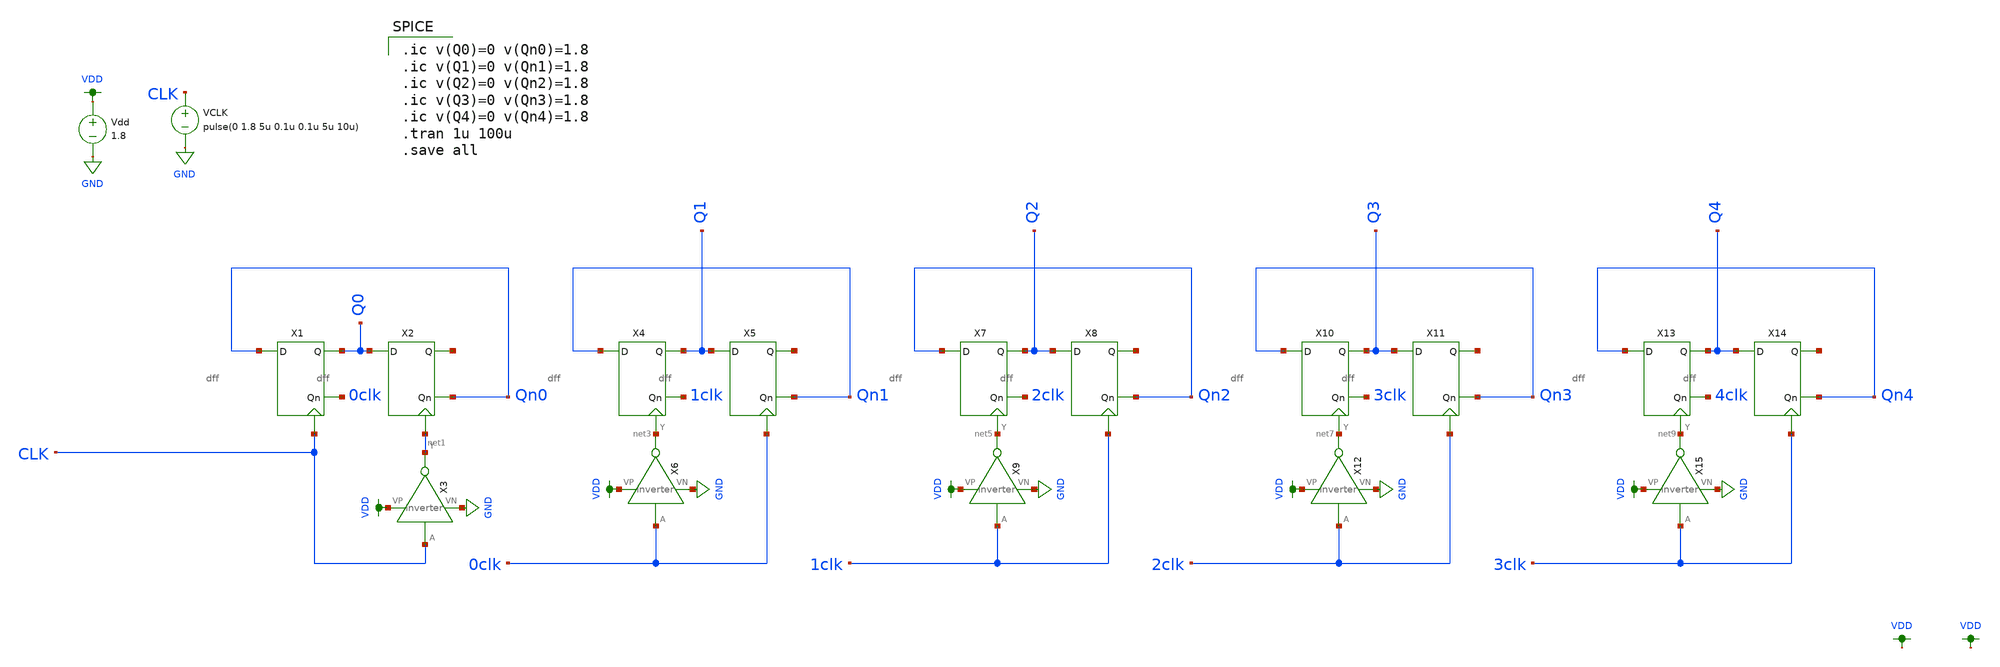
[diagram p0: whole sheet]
** sch_path: schematic/counter_new.sch
**.subckt counter_new
Vdd VDD GND 1.8
VCLK CLK GND pulse(0 1.8 5u 0.1u 0.1u 5u 10u)
X1 Qn0 0clk Q0 CLK dff
X2 Q0 Qn0 net2 net1 dff
X3 CLK net1 VDD GND inverter
X4 Qn1 1clk Q1 net3 dff
X5 Q1 Qn1 net4 0clk dff
X6 0clk net3 VDD GND inverter
X7 Qn2 2clk Q2 net5 dff
X8 Q2 Qn2 net6 1clk dff
X10 Qn3 3clk Q3 net7 dff
X11 Q3 Qn3 net8 2clk dff
X13 Qn4 4clk Q4 net9 dff
X14 Q4 Qn4 net10 3clk dff
X9 1clk net5 VDD GND inverter
X12 2clk net7 VDD GND inverter
X15 3clk net9 VDD GND inverter
**** begin user architecture code

.ic v(Q0)=0 v(Qn0)=1.8
.ic v(Q1)=0 v(Qn1)=1.8
.ic v(Q2)=0 v(Qn2)=1.8
.ic v(Q3)=0 v(Qn3)=1.8
.ic v(Q4)=0 v(Qn4)=1.8
.tran 1u 100u
.save all


.option wnflag=1
.param MC_SWITCH=0.0
.lib ~/skywater/skywater-pdk/libraries/sky130_fd_pr_ngspice/latest/models/sky130.lib.spice tt

**** end user architecture code
**.ends

* expanding   symbol:  /home/madvlsi/Documents/MADVLSI-Final_Project/schematic/dff.sym # of pins=4
** sym_path: schematic/dff.sym
** sch_path: schematic/dff.sch
.subckt dff D Qn Q CLK
*.ipin D
*.iopin CLK
*.opin Qn
*.opin Q
X2 D CLK net1 VDD GND nand2
X3 net3 CLK net2 VDD GND nand2
X4 Q net2 Qn VDD GND nand2
X5 net1 Qn Q VDD GND nand2
X1 D net3 VDD GND inverter
.ends


* expanding   symbol:  /home/madvlsi/Documents/MADVLSI-Final_Project/schematic/inverter.sym # of
*+ pins=4
** sym_path: schematic/inverter.sym
** sch_path: schematic/inverter.sch
.subckt inverter A Y VP VN
*.opin Y
*.ipin A
*.iopin VP
*.iopin VN
XM3 Y A VP VDD sky130_fd_pr__pfet_01v8 L={Lp} W={Wp} nf=1 ad='int((nf+1)/2) * W/nf * 0.29' as='int((nf+2)/2) * W/nf * 0.29'
+ pd='2*int((nf+1)/2) * (W/nf + 0.29)' ps='2*int((nf+2)/2) * (W/nf + 0.29)' nrd='0.29 / W' nrs='0.29 / W'
+ sa=0 sb=0 sd=0 mult=1 m=1
XM4 Y A VP VDD sky130_fd_pr__pfet_01v8 L={Lp} W={Wp} nf=1 ad='int((nf+1)/2) * W/nf * 0.29' as='int((nf+2)/2) * W/nf * 0.29'
+ pd='2*int((nf+1)/2) * (W/nf + 0.29)' ps='2*int((nf+2)/2) * (W/nf + 0.29)' nrd='0.29 / W' nrs='0.29 / W'
+ sa=0 sb=0 sd=0 mult=1 m=1
XM5 Y A VN GND sky130_fd_pr__nfet_01v8 L={Lp} W={Wp} nf=1 ad='int((nf+1)/2) * W/nf * 0.29' as='int((nf+2)/2) * W/nf * 0.29'
+ pd='2*int((nf+1)/2) * (W/nf + 0.29)' ps='2*int((nf+2)/2) * (W/nf + 0.29)' nrd='0.29 / W' nrs='0.29 / W'
+ sa=0 sb=0 sd=0 mult=1 m=1
.ends


* expanding   symbol:  /home/madvlsi/Documents/MADVLSI-Final_Project/schematic/nand2.sym # of pins=5
** sym_path: schematic/nand2.sym
** sch_path: schematic/nand2.sch
.subckt nand2 A B Y VP VN
*.ipin A
*.opin Y
*.ipin B
*.iopin VP
*.iopin VP
*.iopin VN
*.iopin VN
XM1 Y A VP VP sky130_fd_pr__pfet_01v8 L=0.15 W=2 nf=1 ad='int((nf+1)/2) * W/nf * 0.29' as='int((nf+2)/2) * W/nf * 0.29'
+ pd='2*int((nf+1)/2) * (W/nf + 0.29)' ps='2*int((nf+2)/2) * (W/nf + 0.29)' nrd='0.29 / W' nrs='0.29 / W'
+ sa=0 sb=0 sd=0 mult=1 m=1
XM2 VP B Y VP sky130_fd_pr__pfet_01v8 L=0.15 W=2 nf=1 ad='int((nf+1)/2) * W/nf * 0.29' as='int((nf+2)/2) * W/nf * 0.29'
+ pd='2*int((nf+1)/2) * (W/nf + 0.29)' ps='2*int((nf+2)/2) * (W/nf + 0.29)' nrd='0.29 / W' nrs='0.29 / W'
+ sa=0 sb=0 sd=0 mult=1 m=1
XM3 net1 B Y VN sky130_fd_pr__nfet_01v8 L=0.15 W=2 nf=1 ad='int((nf+1)/2) * W/nf * 0.29' as='int((nf+2)/2) * W/nf * 0.29'
+ pd='2*int((nf+1)/2) * (W/nf + 0.29)' ps='2*int((nf+2)/2) * (W/nf + 0.29)' nrd='0.29 / W' nrs='0.29 / W'
+ sa=0 sb=0 sd=0 mult=1 m=1
XM4 net1 A VN VN sky130_fd_pr__nfet_01v8 L=0.15 W=2 nf=1 ad='int((nf+1)/2) * W/nf * 0.29' as='int((nf+2)/2) * W/nf * 0.29'
+ pd='2*int((nf+1)/2) * (W/nf + 0.29)' ps='2*int((nf+2)/2) * (W/nf + 0.29)' nrd='0.29 / W' nrs='0.29 / W'
+ sa=0 sb=0 sd=0 mult=1 m=1
.ends

.GLOBAL GND
.GLOBAL VDD
.end
